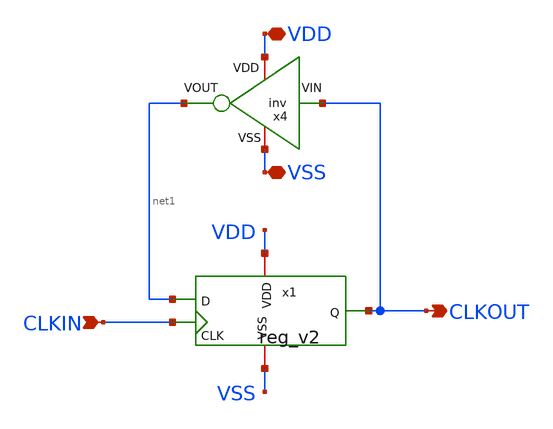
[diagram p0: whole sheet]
** sch_path: design/blocks-std-custom/div_freq_x2/schematic/div_freq_x2.sch
**.subckt div_freq_x2 VDD VSS CLKIN CLKOUT
*.iopin VDD
*.iopin VSS
*.ipin CLKIN
*.opin CLKOUT
x1 VDD CLKIN VSS CLKOUT net1 reg_v2
x4 VDD net1 CLKOUT VSS inv
**.ends
.end
